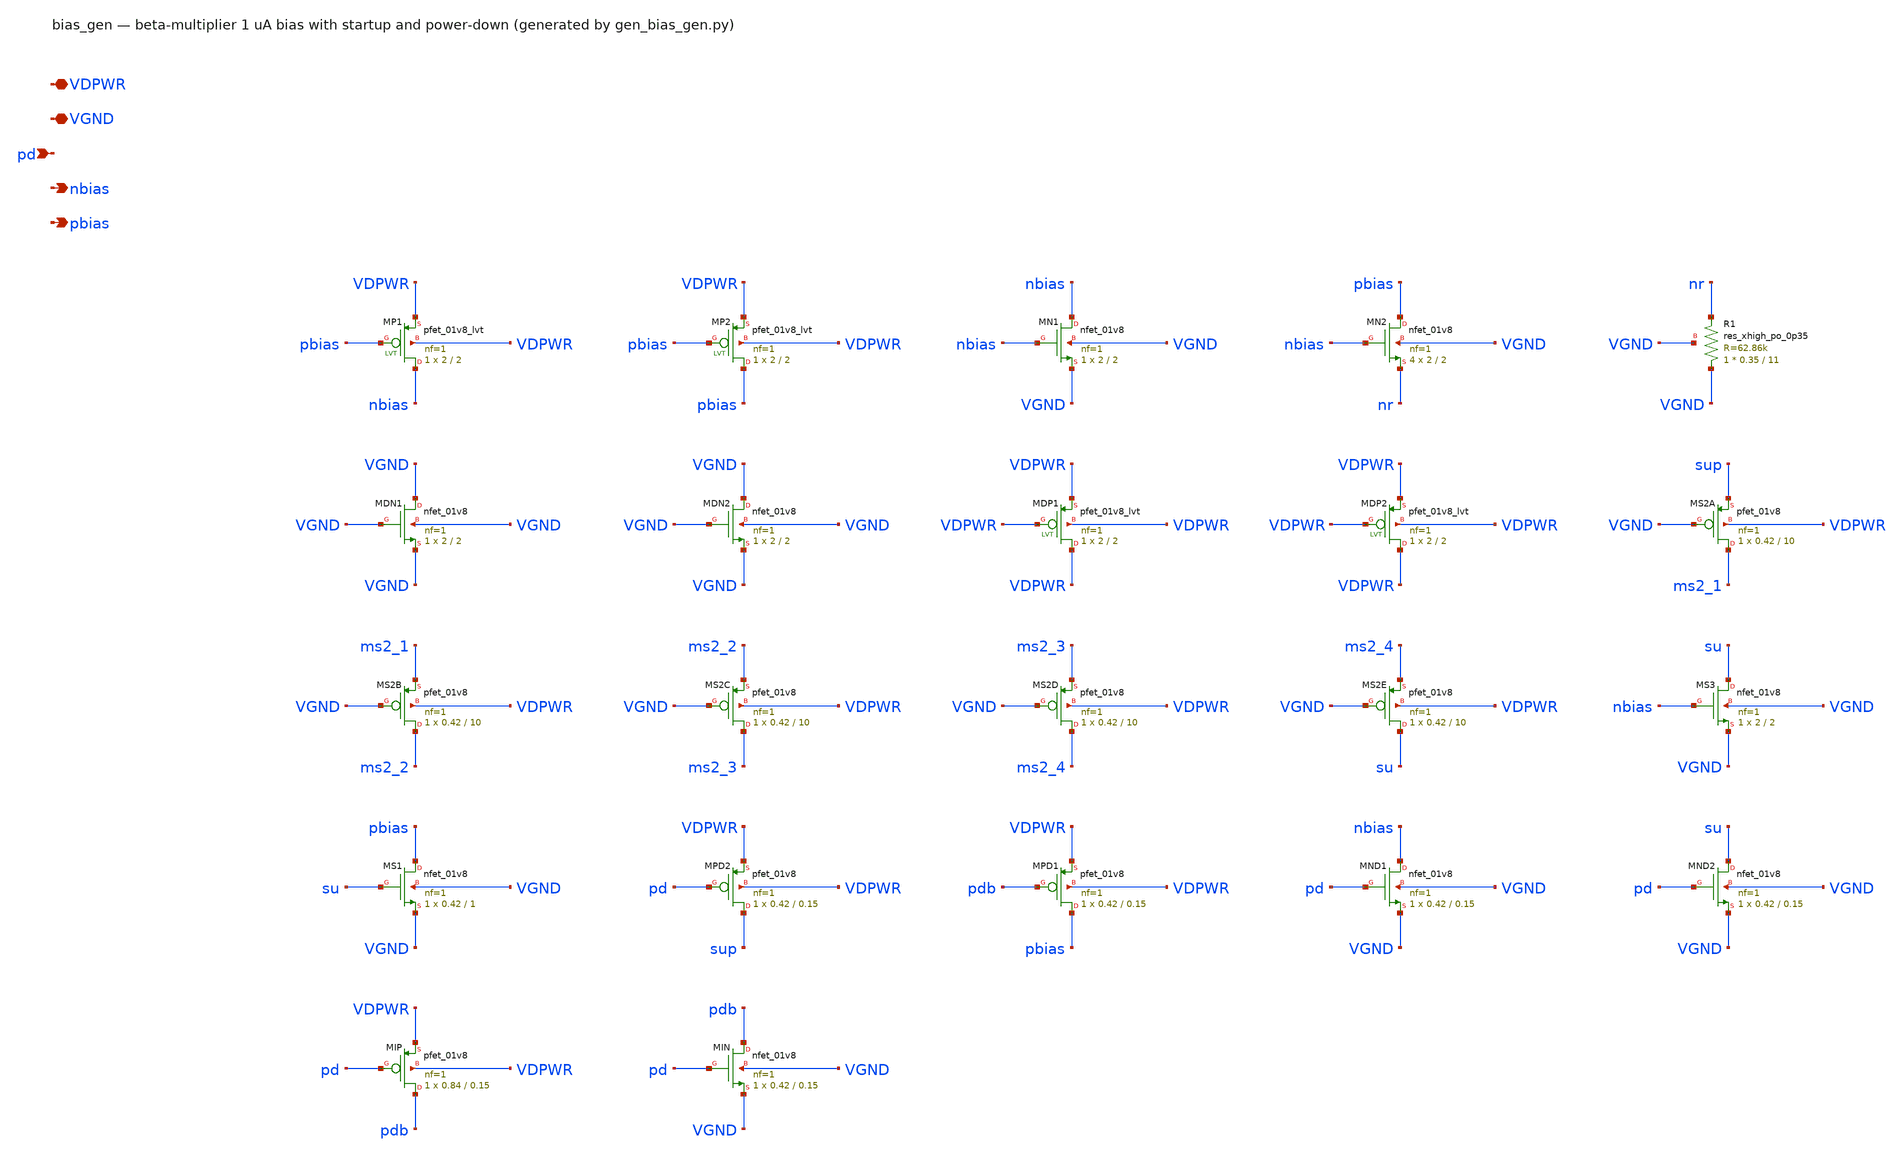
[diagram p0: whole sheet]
** sch_path: xschem/bias_gen.sch
**.subckt bias_gen VDPWR VGND pd nbias pbias
*.iopin VDPWR
*.iopin VGND
*.ipin pd
*.opin nbias
*.opin pbias
XMP1 nbias pbias VDPWR VDPWR sky130_fd_pr__pfet_01v8_lvt L=2 W=2 nf=1 ad='int((1 + 1)/2) * 2 / 1 * 0.29'
+ as='int((1 + 2)/2) * 2 / 1 * 0.29' pd='2*int((1 + 1)/2) * (2 / 1 + 0.29)' ps='2*int((1 + 2)/2) * (2 / 1 + 0.29)'
+ nrd='0.29 / 2 ' nrs='0.29 / 2 ' sa=0 sb=0 sd=0 mult=1 m=1
XMP2 pbias pbias VDPWR VDPWR sky130_fd_pr__pfet_01v8_lvt L=2 W=2 nf=1 ad='int((1 + 1)/2) * 2 / 1 * 0.29'
+ as='int((1 + 2)/2) * 2 / 1 * 0.29' pd='2*int((1 + 1)/2) * (2 / 1 + 0.29)' ps='2*int((1 + 2)/2) * (2 / 1 + 0.29)'
+ nrd='0.29 / 2 ' nrs='0.29 / 2 ' sa=0 sb=0 sd=0 mult=1 m=1
XMN1 nbias nbias VGND VGND sky130_fd_pr__nfet_01v8 L=2 W=2 nf=1 ad='int((1 + 1)/2) * 2 / 1 * 0.29' as='int((1 + 2)/2) * 2 / 1 * 0.29'
+ pd='2*int((1 + 1)/2) * (2 / 1 + 0.29)' ps='2*int((1 + 2)/2) * (2 / 1 + 0.29)' nrd='0.29 / 2 ' nrs='0.29 / 2 '
+ sa=0 sb=0 sd=0 mult=1 m=1
XMN2 pbias nbias nr VGND sky130_fd_pr__nfet_01v8 L=2 W=2 nf=1 ad='int((1 + 1)/2) * 2 / 1 * 0.29' as='int((1 + 2)/2) * 2 / 1 * 0.29'
+ pd='2*int((1 + 1)/2) * (2 / 1 + 0.29)' ps='2*int((1 + 2)/2) * (2 / 1 + 0.29)' nrd='0.29 / 2 ' nrs='0.29 / 2 '
+ sa=0 sb=0 sd=0 mult=4 m=4
XR1 VGND nr VGND sky130_fd_pr__res_xhigh_po_0p35 L=11 mult=1 m=1
XMDN1 VGND VGND VGND VGND sky130_fd_pr__nfet_01v8 L=2 W=2 nf=1 ad='int((1 + 1)/2) * 2 / 1 * 0.29' as='int((1 + 2)/2) * 2 / 1 * 0.29'
+ pd='2*int((1 + 1)/2) * (2 / 1 + 0.29)' ps='2*int((1 + 2)/2) * (2 / 1 + 0.29)' nrd='0.29 / 2 ' nrs='0.29 / 2 '
+ sa=0 sb=0 sd=0 mult=1 m=1
XMDN2 VGND VGND VGND VGND sky130_fd_pr__nfet_01v8 L=2 W=2 nf=1 ad='int((1 + 1)/2) * 2 / 1 * 0.29' as='int((1 + 2)/2) * 2 / 1 * 0.29'
+ pd='2*int((1 + 1)/2) * (2 / 1 + 0.29)' ps='2*int((1 + 2)/2) * (2 / 1 + 0.29)' nrd='0.29 / 2 ' nrs='0.29 / 2 '
+ sa=0 sb=0 sd=0 mult=1 m=1
XMDP1 VDPWR VDPWR VDPWR VDPWR sky130_fd_pr__pfet_01v8_lvt L=2 W=2 nf=1 ad='int((1 + 1)/2) * 2 / 1 * 0.29'
+ as='int((1 + 2)/2) * 2 / 1 * 0.29' pd='2*int((1 + 1)/2) * (2 / 1 + 0.29)' ps='2*int((1 + 2)/2) * (2 / 1 + 0.29)'
+ nrd='0.29 / 2 ' nrs='0.29 / 2 ' sa=0 sb=0 sd=0 mult=1 m=1
XMDP2 VDPWR VDPWR VDPWR VDPWR sky130_fd_pr__pfet_01v8_lvt L=2 W=2 nf=1 ad='int((1 + 1)/2) * 2 / 1 * 0.29'
+ as='int((1 + 2)/2) * 2 / 1 * 0.29' pd='2*int((1 + 1)/2) * (2 / 1 + 0.29)' ps='2*int((1 + 2)/2) * (2 / 1 + 0.29)'
+ nrd='0.29 / 2 ' nrs='0.29 / 2 ' sa=0 sb=0 sd=0 mult=1 m=1
XMS2A ms2_1 VGND sup VDPWR sky130_fd_pr__pfet_01v8 L=10 W=0.42 nf=1 ad='int((nf+1)/2) * W/nf * 0.29'
+ as='int((nf+2)/2) * W/nf * 0.29' pd='2*int((nf+1)/2) * (W/nf + 0.29)' ps='2*int((nf+2)/2) * (W/nf + 0.29)'
+ nrd='0.29 / W' nrs='0.29 / W' sa=0 sb=0 sd=0 mult=1 m=1
XMS2B ms2_2 VGND ms2_1 VDPWR sky130_fd_pr__pfet_01v8 L=10 W=0.42 nf=1 ad='int((nf+1)/2) * W/nf * 0.29'
+ as='int((nf+2)/2) * W/nf * 0.29' pd='2*int((nf+1)/2) * (W/nf + 0.29)' ps='2*int((nf+2)/2) * (W/nf + 0.29)'
+ nrd='0.29 / W' nrs='0.29 / W' sa=0 sb=0 sd=0 mult=1 m=1
XMS2C ms2_3 VGND ms2_2 VDPWR sky130_fd_pr__pfet_01v8 L=10 W=0.42 nf=1 ad='int((nf+1)/2) * W/nf * 0.29'
+ as='int((nf+2)/2) * W/nf * 0.29' pd='2*int((nf+1)/2) * (W/nf + 0.29)' ps='2*int((nf+2)/2) * (W/nf + 0.29)'
+ nrd='0.29 / W' nrs='0.29 / W' sa=0 sb=0 sd=0 mult=1 m=1
XMS2D ms2_4 VGND ms2_3 VDPWR sky130_fd_pr__pfet_01v8 L=10 W=0.42 nf=1 ad='int((nf+1)/2) * W/nf * 0.29'
+ as='int((nf+2)/2) * W/nf * 0.29' pd='2*int((nf+1)/2) * (W/nf + 0.29)' ps='2*int((nf+2)/2) * (W/nf + 0.29)'
+ nrd='0.29 / W' nrs='0.29 / W' sa=0 sb=0 sd=0 mult=1 m=1
XMS2E su VGND ms2_4 VDPWR sky130_fd_pr__pfet_01v8 L=10 W=0.42 nf=1 ad='int((nf+1)/2) * W/nf * 0.29' as='int((nf+2)/2) * W/nf * 0.29'
+ pd='2*int((nf+1)/2) * (W/nf + 0.29)' ps='2*int((nf+2)/2) * (W/nf + 0.29)' nrd='0.29 / W' nrs='0.29 / W'
+ sa=0 sb=0 sd=0 mult=1 m=1
XMS3 su nbias VGND VGND sky130_fd_pr__nfet_01v8 L=2 W=2 nf=1 ad='int((1 + 1)/2) * 2 / 1 * 0.29' as='int((1 + 2)/2) * 2 / 1 * 0.29'
+ pd='2*int((1 + 1)/2) * (2 / 1 + 0.29)' ps='2*int((1 + 2)/2) * (2 / 1 + 0.29)' nrd='0.29 / 2 ' nrs='0.29 / 2 '
+ sa=0 sb=0 sd=0 mult=1 m=1
XMS1 pbias su VGND VGND sky130_fd_pr__nfet_01v8 L=1 W=0.42 nf=1 ad='int((1 + 1)/2) * 0.42 / 1 * 0.29'
+ as='int((1 + 2)/2) * 0.42 / 1 * 0.29' pd='2*int((1 + 1)/2) * (0.42 / 1 + 0.29)' ps='2*int((1 + 2)/2) * (0.42 / 1 + 0.29)'
+ nrd='0.29 / 0.42 ' nrs='0.29 / 0.42 ' sa=0 sb=0 sd=0 mult=1 m=1
XMPD2 sup pd VDPWR VDPWR sky130_fd_pr__pfet_01v8 L=0.15 W=0.42 nf=1 ad='int((nf+1)/2) * W/nf * 0.29'
+ as='int((nf+2)/2) * W/nf * 0.29' pd='2*int((nf+1)/2) * (W/nf + 0.29)' ps='2*int((nf+2)/2) * (W/nf + 0.29)'
+ nrd='0.29 / W' nrs='0.29 / W' sa=0 sb=0 sd=0 mult=1 m=1
XMPD1 pbias pdb VDPWR VDPWR sky130_fd_pr__pfet_01v8 L=0.15 W=0.42 nf=1 ad='int((nf+1)/2) * W/nf * 0.29'
+ as='int((nf+2)/2) * W/nf * 0.29' pd='2*int((nf+1)/2) * (W/nf + 0.29)' ps='2*int((nf+2)/2) * (W/nf + 0.29)'
+ nrd='0.29 / W' nrs='0.29 / W' sa=0 sb=0 sd=0 mult=1 m=1
XMND1 nbias pd VGND VGND sky130_fd_pr__nfet_01v8 L=0.15 W=0.42 nf=1 ad='int((1 + 1)/2) * 0.42 / 1 * 0.29'
+ as='int((1 + 2)/2) * 0.42 / 1 * 0.29' pd='2*int((1 + 1)/2) * (0.42 / 1 + 0.29)' ps='2*int((1 + 2)/2) * (0.42 / 1 + 0.29)'
+ nrd='0.29 / 0.42 ' nrs='0.29 / 0.42 ' sa=0 sb=0 sd=0 mult=1 m=1
XMND2 su pd VGND VGND sky130_fd_pr__nfet_01v8 L=0.15 W=0.42 nf=1 ad='int((1 + 1)/2) * 0.42 / 1 * 0.29'
+ as='int((1 + 2)/2) * 0.42 / 1 * 0.29' pd='2*int((1 + 1)/2) * (0.42 / 1 + 0.29)' ps='2*int((1 + 2)/2) * (0.42 / 1 + 0.29)'
+ nrd='0.29 / 0.42 ' nrs='0.29 / 0.42 ' sa=0 sb=0 sd=0 mult=1 m=1
XMIP pdb pd VDPWR VDPWR sky130_fd_pr__pfet_01v8 L=0.15 W=0.84 nf=1 ad='int((nf+1)/2) * W/nf * 0.29' as='int((nf+2)/2) * W/nf * 0.29'
+ pd='2*int((nf+1)/2) * (W/nf + 0.29)' ps='2*int((nf+2)/2) * (W/nf + 0.29)' nrd='0.29 / W' nrs='0.29 / W'
+ sa=0 sb=0 sd=0 mult=1 m=1
XMIN pdb pd VGND VGND sky130_fd_pr__nfet_01v8 L=0.15 W=0.42 nf=1 ad='int((1 + 1)/2) * 0.42 / 1 * 0.29'
+ as='int((1 + 2)/2) * 0.42 / 1 * 0.29' pd='2*int((1 + 1)/2) * (0.42 / 1 + 0.29)' ps='2*int((1 + 2)/2) * (0.42 / 1 + 0.29)'
+ nrd='0.29 / 0.42 ' nrs='0.29 / 0.42 ' sa=0 sb=0 sd=0 mult=1 m=1
**.ends
.end
